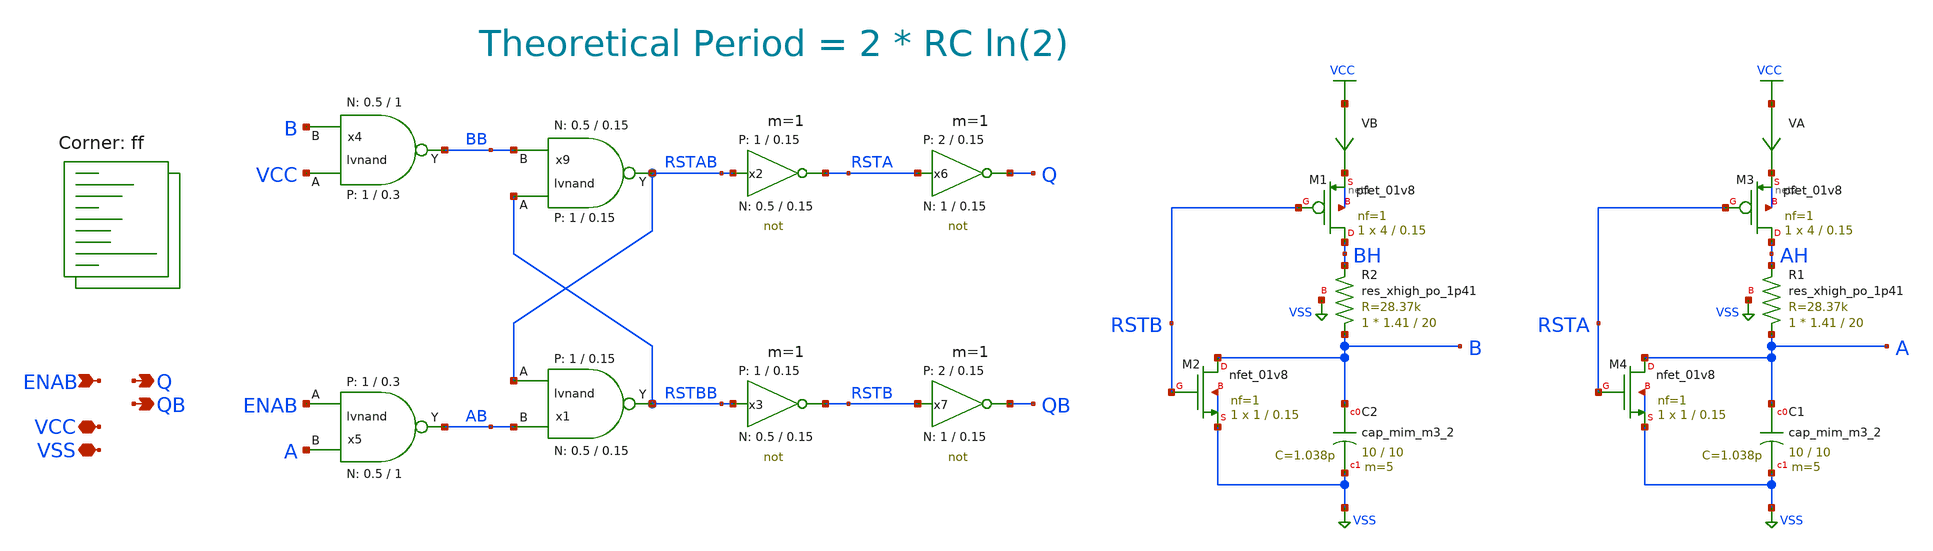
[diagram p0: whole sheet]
** sch_path: sky130A/xschem_libs/sky130_tests/sky130_oscillator/schematic/sky130_oscillator.sch
* StefanSchippers/xschem_sky130/sky130_tests/lvnand.sch:
* Copyright 2021 Stefan Frederik Schippers
* Licensed under the Apache License, Version 2.0 (the "License");
**.subckt sky130_oscillator VSS VCC ENAB QB Q
*.iopin VSS
*.iopin VCC
*.ipin ENAB
*.opin QB
*.opin Q
x9 RSTBB BB RSTAB VCC VSS lvnand WidthN=0.5 LenN=0.15 WidthP=1 LenP=0.15 m=1
x1 RSTAB AB RSTBB VCC VSS lvnand WidthN=0.5 LenN=0.15 WidthP=1 LenP=0.15 m=1
XM1 BH RSTB net1 net1 sky130_fd_pr__pfet_01v8 L=0.15 W=4 nf=1 ad='int((nf+1)/2) * W/nf * 0.29' as='int((nf+2)/2) * W/nf * 0.29'
+ pd='2*int((nf+1)/2) * (W/nf + 0.29)' ps='2*int((nf+2)/2) * (W/nf + 0.29)' nrd='0.29 / W' nrs='0.29 / W'
+ sa=0 sb=0 sd=0 mult=1 m=1
XM2 B RSTB VSS VSS sky130_fd_pr__nfet_01v8 L=0.15 W=1 nf=1 ad='int((1 + 1)/2) * 1 / 1 * 0.29' as='int((1 + 2)/2) * 1 / 1 * 0.29'
+ pd='2*int((1 + 1)/2) * (1 / 1 + 0.29)' ps='2*int((1 + 2)/2) * (1 / 1 + 0.29)' nrd='0.29 / 1 ' nrs='0.29 / 1 '
+ sa=0 sb=0 sd=0 mult=1 m=1
x2 RSTA RSTAB VCC VSS not W_N=0.5 L_N=0.15 W_P=1 L_P=0.15 m=1
x3 RSTB RSTBB VCC VSS not W_N=0.5 L_N=0.15 W_P=1 L_P=0.15 m=1
x4 VCC B BB VCC VSS lvnand WidthN=0.5 LenN=1 WidthP=1 LenP=0.3 m=1
x5 ENAB A AB VCC VSS lvnand WidthN=0.5 LenN=1 WidthP=1 LenP=0.3 m=1
XM3 AH RSTA net2 net2 sky130_fd_pr__pfet_01v8 L=0.15 W=4 nf=1 ad='int((nf+1)/2) * W/nf * 0.29' as='int((nf+2)/2) * W/nf * 0.29'
+ pd='2*int((nf+1)/2) * (W/nf + 0.29)' ps='2*int((nf+2)/2) * (W/nf + 0.29)' nrd='0.29 / W' nrs='0.29 / W'
+ sa=0 sb=0 sd=0 mult=1 m=1
XM4 A RSTA VSS VSS sky130_fd_pr__nfet_01v8 L=0.15 W=1 nf=1 ad='int((1 + 1)/2) * 1 / 1 * 0.29' as='int((1 + 2)/2) * 1 / 1 * 0.29'
+ pd='2*int((1 + 1)/2) * (1 / 1 + 0.29)' ps='2*int((1 + 2)/2) * (1 / 1 + 0.29)' nrd='0.29 / 1 ' nrs='0.29 / 1 '
+ sa=0 sb=0 sd=0 mult=1 m=1
x6 Q RSTA VCC VSS not W_N=1 L_N=0.15 W_P=2 L_P=0.15 m=1
x7 QB RSTB VCC VSS not W_N=1 L_N=0.15 W_P=2 L_P=0.15 m=1
XC2 B VSS sky130_fd_pr__cap_mim_m3_2 W=10 L=10 MF=5 m=5
XC1 A VSS sky130_fd_pr__cap_mim_m3_2 W=10 L=10 MF=5 m=5
XR1 A AH VSS sky130_fd_pr__res_xhigh_po_1p41 L=20 mult=1 m=1
XR2 B BH VSS sky130_fd_pr__res_xhigh_po_1p41 L=20 mult=1 m=1
VB VCC net1 0
VA VCC net2 0
**** begin user architecture code


.param VCC=1.7
.option savecurrents method=gear
.save all
vvcc vcc 0 'VCC'
vvss vss 0 0
venab enab 0 pwl 0 0 100n 0 101n 'VCC'500n 'VCC' 501n 0
.control
  tran 0.04n 600n
  remzerovec
  plot @m.x4.xm1.msky130_fd_pr__nfet_01v8[id] @m.x5.xm1.msky130_fd_pr__nfet_01v8[id]
  write sky130_oscillator.raw
  alterparam vcc=1.9
  reset
  set appendwrite
  tran 0.04n 600n
  plot @m.x4.xm1.msky130_fd_pr__nfet_01v8[id] @m.x5.xm1.msky130_fd_pr__nfet_01v8[id]
  remzerovec
  write sky130_oscillator.raw
.endc


.lib $::SKYWATER_MODELS/sky130.lib.spice ff
**** end user architecture code
**.ends

* expanding   symbol:  sky130_tests/lvnand.sym # of pins=3
** sym_path: sky130_tests/lvnand.sym
** sch_path: sky130_tests/lvnand.sch
.subckt lvnand A B Y VCCPIN VSSPIN  WidthN=1 LenN=0.15 WidthP=1 LenP=0.15
*.ipin A
*.ipin B
*.opin Y
XM1 Y B S VSSPIN sky130_fd_pr__nfet_01v8 L=LenN W=WidthN nf=1 ad='int((nf+1)/2) * W/nf * 0.29' as='int((nf+2)/2) * W/nf * 0.29'
+ pd='2*int((nf+1)/2) * (W/nf + 0.29)' ps='2*int((nf+2)/2) * (W/nf + 0.29)' nrd='0.29 / W' nrs='0.29 / W'
+ sa=0 sb=0 sd=0 mult=1 m=1
XM2 Y A VCCPIN VCCPIN sky130_fd_pr__pfet_01v8 L=LenP W=WidthP nf=1 ad='int((nf+1)/2) * W/nf * 0.29' as='int((nf+2)/2) * W/nf * 0.29'
+ pd='2*int((nf+1)/2) * (W/nf + 0.29)' ps='2*int((nf+2)/2) * (W/nf + 0.29)' nrd='0.29 / W' nrs='0.29 / W'
+ sa=0 sb=0 sd=0 mult=1 m=1
XM3 Y B VCCPIN VCCPIN sky130_fd_pr__pfet_01v8 L=LenP W=WidthP nf=1 ad='int((nf+1)/2) * W/nf * 0.29' as='int((nf+2)/2) * W/nf * 0.29'
+ pd='2*int((nf+1)/2) * (W/nf + 0.29)' ps='2*int((nf+2)/2) * (W/nf + 0.29)' nrd='0.29 / W' nrs='0.29 / W'
+ sa=0 sb=0 sd=0 mult=1 m=1
XM4 S A VSSPIN VSSPIN sky130_fd_pr__nfet_01v8 L=LenN W=WidthN nf=1 ad='int((nf+1)/2) * W/nf * 0.29' as='int((nf+2)/2) * W/nf * 0.29'
+ pd='2*int((nf+1)/2) * (W/nf + 0.29)' ps='2*int((nf+2)/2) * (W/nf + 0.29)' nrd='0.29 / W' nrs='0.29 / W'
+ sa=0 sb=0 sd=0 mult=1 m=1
.ends


* expanding   symbol:  sky130_tests/not.sym # of pins=2
** sym_path: sky130_tests/not.sym
** sch_path: sky130_tests/not.sch
.subckt not y a VCCPIN VSSPIN     W_N=1 L_N=0.15 W_P=2 L_P=0.15
*.opin y
*.ipin a
XM1 DN a VSSPIN VSSPIN sky130_fd_pr__nfet_01v8 L=L_N W=W_N nf=1 ad='int((1 + 1)/2) * W_N / 1 * 0.29'
+ as='int((1 + 2)/2) * W_N / 1 * 0.29' pd='2*int((1 + 1)/2) * (W_N / 1 + 0.29)' ps='2*int((1 + 2)/2) * (W_N / 1 + 0.29)'
+ nrd='0.29 / W_N ' nrs='0.29 / W_N ' sa=0 sb=0 sd=0 mult=1 m=1
XM2 DP a VCCPIN VCCPIN sky130_fd_pr__pfet_01v8 L=L_P W=W_P nf=1 ad='int((nf+1)/2) * W/nf * 0.29' as='int((nf+2)/2) * W/nf * 0.29'
+ pd='2*int((nf+1)/2) * (W/nf + 0.29)' ps='2*int((nf+2)/2) * (W/nf + 0.29)' nrd='0.29 / W' nrs='0.29 / W'
+ sa=0 sb=0 sd=0 mult=1 m=1
Vmeas DP y 0
.save i(vmeas)
Vmeas1 y DN 0
.save i(vmeas1)
.save v(dp)
.save v(dn)
.ends

.GLOBAL VCC
.GLOBAL VSS
.end
